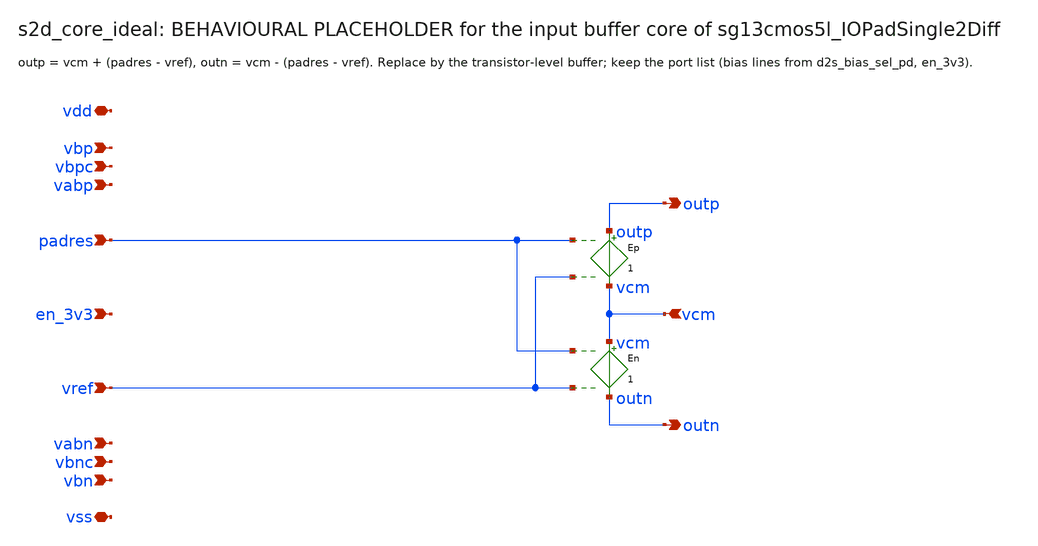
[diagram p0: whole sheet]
** sch_path: sudelbuecher/design_considerations/consolidation/bias_hierarchy_2026-10-27/before/macros/sg13cmos5l_IOPadSingle2Diff/schematic/xschem/s2d_core_ideal.sch
**.subckt s2d_core_ideal vdd vss padres vref vcm outp outn vbp vbn vbpc vbnc vabp vabn en_3v3
*.iopin vdd
*.iopin vss
*.ipin padres
*.ipin vref
*.ipin vcm
*.opin outp
*.opin outn
*.ipin vbp
*.ipin vbn
*.ipin vbpc
*.ipin vbnc
*.ipin vabp
*.ipin vabn
*.ipin en_3v3
Ep outp vcm padres vref 1
En vcm outn padres vref 1
**.ends
.end
